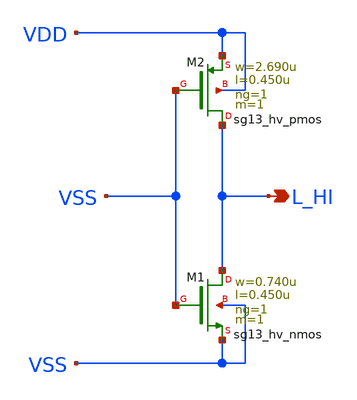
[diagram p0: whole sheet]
** sch_path: ihp-sg13g2/libs.ref/sg13g2_stdcell_hv/sch/xschem/sg13g2_hv_tiehi.sch
* Copyright 2023 IHP PDK Authors
* Licensed under the Apache License, Version 2.0 (the "License");
* you may not use this file except in compliance with the License.
* You may obtain a copy of the License at
* https://www.apache.org/licenses/LICENSE-2.0
* Unless required by applicable law or agreed to in writing, software
* distributed under the License is distributed on an "AS IS" BASIS,
* WITHOUT WARRANTIES OR CONDITIONS OF ANY KIND, either express or implied.
* See the License for the specific language governing permissions and
* limitations under the License.
**.subckt sg13g2_hv_tiehi L_HI
*.opin L_HI
XM1 L_HI VSS VSS VSS sg13_hv_nmos w=0.740u l=0.450u ng=1 m=1 mm_ok=1
XM2 L_HI VSS VDD VDD sg13_hv_pmos w=2.690u l=0.450u ng=1 m=1 mm_ok=1
**.ends
.end
